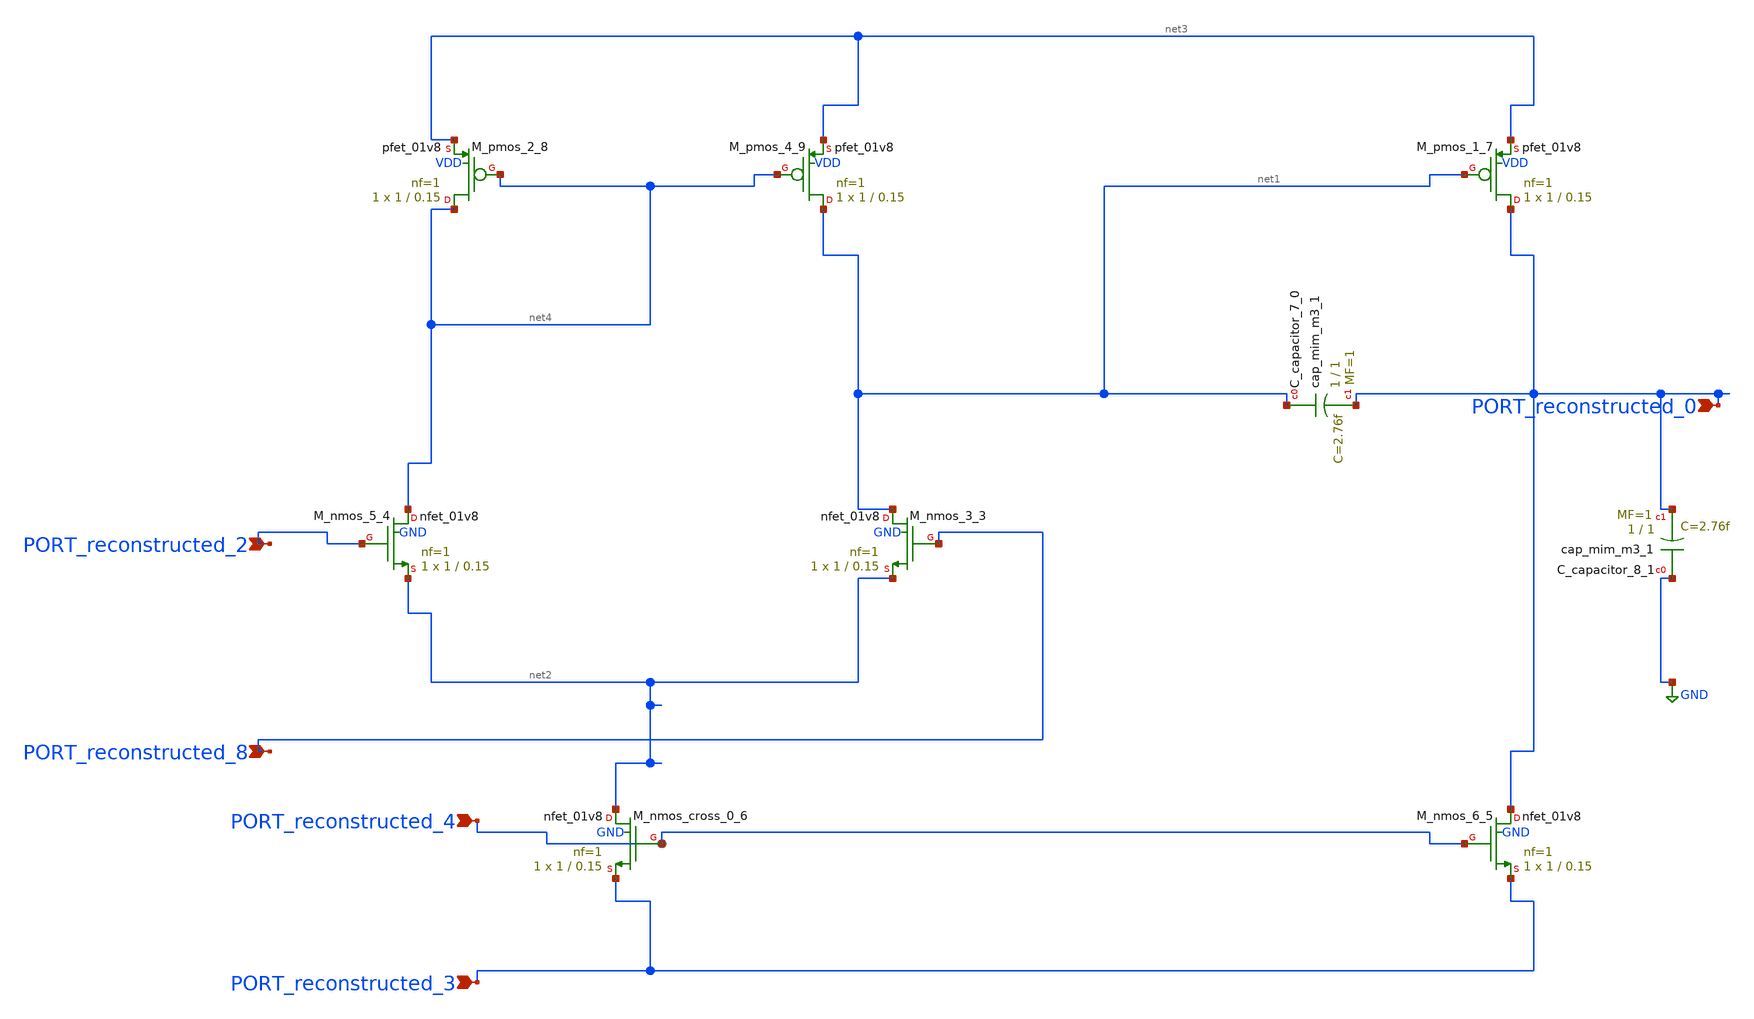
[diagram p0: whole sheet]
** sch_path: schematics/Image2Net/066.sch
**.subckt 066 PORT_reconstructed_8 PORT_reconstructed_0 PORT_reconstructed_2 PORT_reconstructed_4
*+ PORT_reconstructed_3
*.ipin PORT_reconstructed_8
*.ipin PORT_reconstructed_0
*.ipin PORT_reconstructed_2
*.ipin PORT_reconstructed_4
*.ipin PORT_reconstructed_3
XC_capacitor_7_0 net1 PORT_reconstructed_0 sky130_fd_pr__cap_mim_m3_1 W=1 L=1 MF=1 m=1
XC_capacitor_8_1 GND PORT_reconstructed_0 sky130_fd_pr__cap_mim_m3_1 W=1 L=1 MF=1 m=1
XM_nmos_3_3 net1 PORT_reconstructed_8 net2 GND sky130_fd_pr__nfet_01v8 L=0.15 W=1 nf=1 ad='int((1 + 1)/2) * 1 / 1 * 0.29'
+ as='int((1 + 2)/2) * 1 / 1 * 0.29' pd='2*int((1 + 1)/2) * (1 / 1 + 0.29)' ps='2*int((1 + 2)/2) * (1 / 1 + 0.29)'
+ nrd='0.29 / 1 ' nrs='0.29 / 1 ' sa=0 sb=0 sd=0 mult=1 m=1
XM_nmos_5_4 net4 PORT_reconstructed_2 net2 GND sky130_fd_pr__nfet_01v8 L=0.15 W=1 nf=1 ad='int((1 + 1)/2) * 1 / 1 * 0.29'
+ as='int((1 + 2)/2) * 1 / 1 * 0.29' pd='2*int((1 + 1)/2) * (1 / 1 + 0.29)' ps='2*int((1 + 2)/2) * (1 / 1 + 0.29)'
+ nrd='0.29 / 1 ' nrs='0.29 / 1 ' sa=0 sb=0 sd=0 mult=1 m=1
XM_nmos_6_5 PORT_reconstructed_0 PORT_reconstructed_4 PORT_reconstructed_3 GND sky130_fd_pr__nfet_01v8
+ L=0.15 W=1 nf=1 ad='int((1 + 1)/2) * 1 / 1 * 0.29' as='int((1 + 2)/2) * 1 / 1 * 0.29' pd='2*int((1 + 1)/2) * (1 / 1 + 0.29)'
+ ps='2*int((1 + 2)/2) * (1 / 1 + 0.29)' nrd='0.29 / 1 ' nrs='0.29 / 1 ' sa=0 sb=0 sd=0 mult=1 m=1
XM_nmos_cross_0_6 net2 PORT_reconstructed_4 PORT_reconstructed_3 GND sky130_fd_pr__nfet_01v8 L=0.15 W=1
+ nf=1 ad='int((1 + 1)/2) * 1 / 1 * 0.29' as='int((1 + 2)/2) * 1 / 1 * 0.29' pd='2*int((1 + 1)/2) * (1 / 1 + 0.29)'
+ ps='2*int((1 + 2)/2) * (1 / 1 + 0.29)' nrd='0.29 / 1 ' nrs='0.29 / 1 ' sa=0 sb=0 sd=0 mult=1 m=1
XM_pmos_1_7 PORT_reconstructed_0 net1 net3 VDD sky130_fd_pr__pfet_01v8 L=0.15 W=1 nf=1 ad='int((1 + 1)/2) * 1 / 1 * 0.29'
+ as='int((1 + 2)/2) * 1 / 1 * 0.29' pd='2*int((1 + 1)/2) * (1 / 1 + 0.29)' ps='2*int((1 + 2)/2) * (1 / 1 + 0.29)'
+ nrd='0.29 / 1 ' nrs='0.29 / 1 ' sa=0 sb=0 sd=0 mult=1 m=1
XM_pmos_2_8 net4 net4 net3 VDD sky130_fd_pr__pfet_01v8 L=0.15 W=1 nf=1 ad='int((1 + 1)/2) * 1 / 1 * 0.29'
+ as='int((1 + 2)/2) * 1 / 1 * 0.29' pd='2*int((1 + 1)/2) * (1 / 1 + 0.29)' ps='2*int((1 + 2)/2) * (1 / 1 + 0.29)'
+ nrd='0.29 / 1 ' nrs='0.29 / 1 ' sa=0 sb=0 sd=0 mult=1 m=1
XM_pmos_4_9 net1 net4 net3 VDD sky130_fd_pr__pfet_01v8 L=0.15 W=1 nf=1 ad='int((1 + 1)/2) * 1 / 1 * 0.29'
+ as='int((1 + 2)/2) * 1 / 1 * 0.29' pd='2*int((1 + 1)/2) * (1 / 1 + 0.29)' ps='2*int((1 + 2)/2) * (1 / 1 + 0.29)'
+ nrd='0.29 / 1 ' nrs='0.29 / 1 ' sa=0 sb=0 sd=0 mult=1 m=1
**.ends
.GLOBAL GND
.end
